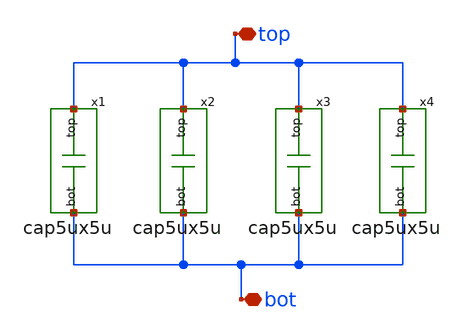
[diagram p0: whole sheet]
** sch_path: v2_feature_extr/cap20ux20u.sch
**.subckt cap20ux20u top bot
*.iopin top
*.iopin bot
x1 top bot cap5ux5u
x2 top bot cap5ux5u
x3 top bot cap5ux5u
x4 top bot cap5ux5u
**.ends
.end
